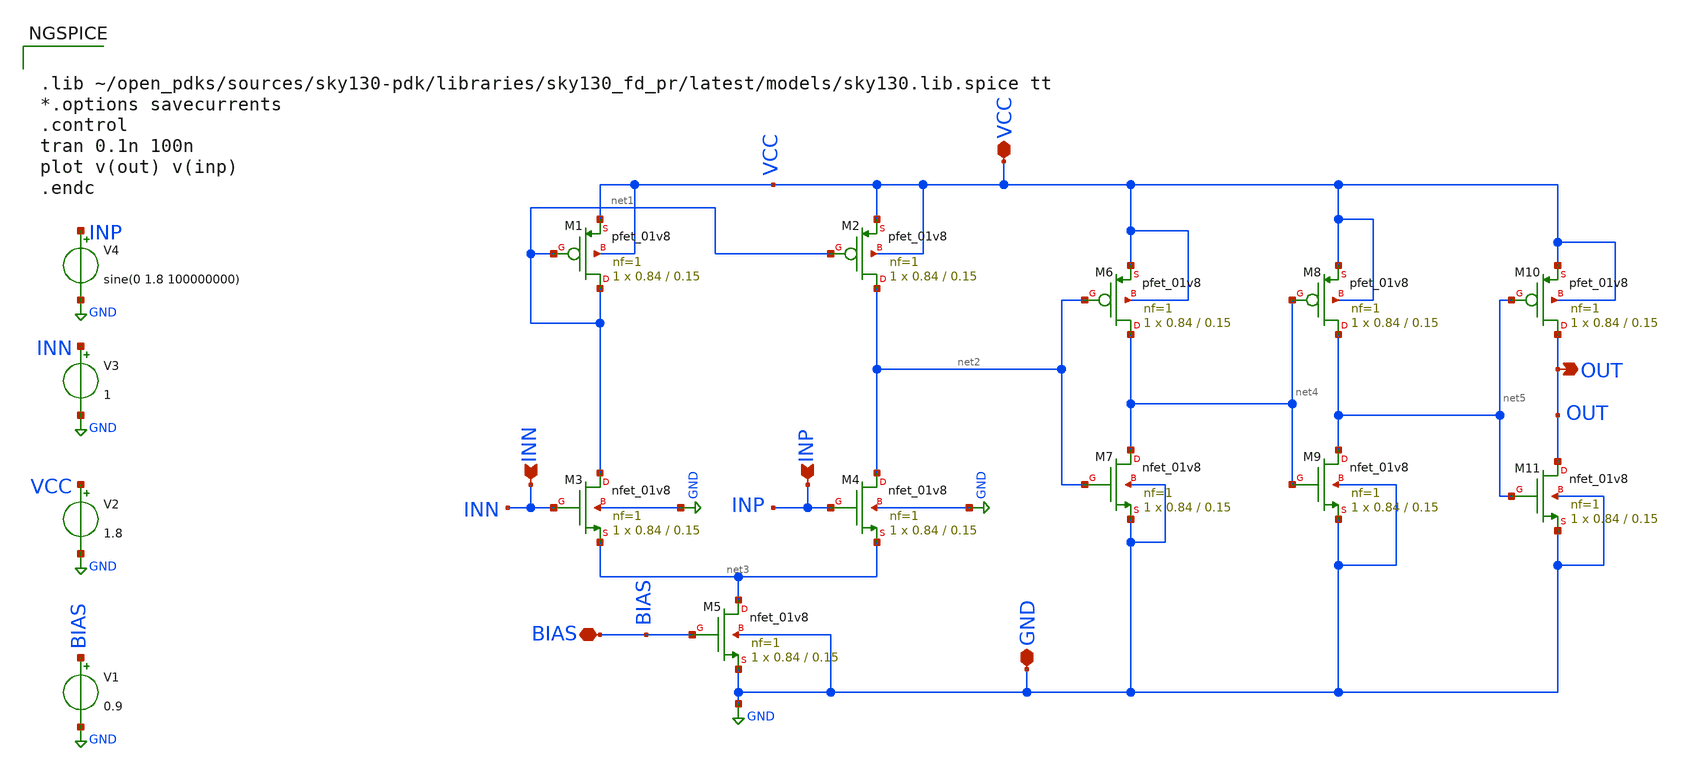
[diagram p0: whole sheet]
** sch_path: Week 4/xschem_180/comp_150.sch
**.subckt comp_150 OUT VCC GND INP INN BIAS
*.opin OUT
*.iopin VCC
*.iopin GND
*.ipin INP
*.ipin INN
*.iopin BIAS
V2 VCC GND 1.8
V3 INN GND 1
V4 INP GND sine(0 1.8 100000000)
XM1 net1 net1 VCC VCC sky130_fd_pr__pfet_01v8 L=0.15 W=0.84 nf=1 ad='int((nf+1)/2) * W/nf * 0.29' as='int((nf+2)/2) * W/nf * 0.29'
+ pd='2*int((nf+1)/2) * (W/nf + 0.29)' ps='2*int((nf+2)/2) * (W/nf + 0.29)' nrd='0.29 / W' nrs='0.29 / W'
+ sa=0 sb=0 sd=0 mult=1 m=1
XM2 net2 net1 VCC VCC sky130_fd_pr__pfet_01v8 L=0.15 W=0.84 nf=1 ad='int((nf+1)/2) * W/nf * 0.29' as='int((nf+2)/2) * W/nf * 0.29'
+ pd='2*int((nf+1)/2) * (W/nf + 0.29)' ps='2*int((nf+2)/2) * (W/nf + 0.29)' nrd='0.29 / W' nrs='0.29 / W'
+ sa=0 sb=0 sd=0 mult=1 m=1
XM3 net1 INN net3 GND sky130_fd_pr__nfet_01v8 L=0.15 W=0.84 nf=1 ad='int((nf+1)/2) * W/nf * 0.29' as='int((nf+2)/2) * W/nf * 0.29'
+ pd='2*int((nf+1)/2) * (W/nf + 0.29)' ps='2*int((nf+2)/2) * (W/nf + 0.29)' nrd='0.29 / W' nrs='0.29 / W'
+ sa=0 sb=0 sd=0 mult=1 m=1
XM4 net2 INP net3 GND sky130_fd_pr__nfet_01v8 L=0.15 W=0.84 nf=1 ad='int((nf+1)/2) * W/nf * 0.29' as='int((nf+2)/2) * W/nf * 0.29'
+ pd='2*int((nf+1)/2) * (W/nf + 0.29)' ps='2*int((nf+2)/2) * (W/nf + 0.29)' nrd='0.29 / W' nrs='0.29 / W'
+ sa=0 sb=0 sd=0 mult=1 m=1
XM5 net3 BIAS GND GND sky130_fd_pr__nfet_01v8 L=0.15 W=0.84 nf=1 ad='int((nf+1)/2) * W/nf * 0.29' as='int((nf+2)/2) * W/nf * 0.29'
+ pd='2*int((nf+1)/2) * (W/nf + 0.29)' ps='2*int((nf+2)/2) * (W/nf + 0.29)' nrd='0.29 / W' nrs='0.29 / W'
+ sa=0 sb=0 sd=0 mult=1 m=1
V1 BIAS GND 0.9
XM6 net4 net2 VCC VCC sky130_fd_pr__pfet_01v8 L=0.15 W=0.84 nf=1 ad='int((nf+1)/2) * W/nf * 0.29' as='int((nf+2)/2) * W/nf * 0.29'
+ pd='2*int((nf+1)/2) * (W/nf + 0.29)' ps='2*int((nf+2)/2) * (W/nf + 0.29)' nrd='0.29 / W' nrs='0.29 / W'
+ sa=0 sb=0 sd=0 mult=1 m=1
XM7 net4 net2 GND GND sky130_fd_pr__nfet_01v8 L=0.15 W=0.84 nf=1 ad='int((nf+1)/2) * W/nf * 0.29' as='int((nf+2)/2) * W/nf * 0.29'
+ pd='2*int((nf+1)/2) * (W/nf + 0.29)' ps='2*int((nf+2)/2) * (W/nf + 0.29)' nrd='0.29 / W' nrs='0.29 / W'
+ sa=0 sb=0 sd=0 mult=1 m=1
XM8 net5 net4 VCC VCC sky130_fd_pr__pfet_01v8 L=0.15 W=0.84 nf=1 ad='int((nf+1)/2) * W/nf * 0.29' as='int((nf+2)/2) * W/nf * 0.29'
+ pd='2*int((nf+1)/2) * (W/nf + 0.29)' ps='2*int((nf+2)/2) * (W/nf + 0.29)' nrd='0.29 / W' nrs='0.29 / W'
+ sa=0 sb=0 sd=0 mult=1 m=1
XM9 net5 net4 GND GND sky130_fd_pr__nfet_01v8 L=0.15 W=0.84 nf=1 ad='int((nf+1)/2) * W/nf * 0.29' as='int((nf+2)/2) * W/nf * 0.29'
+ pd='2*int((nf+1)/2) * (W/nf + 0.29)' ps='2*int((nf+2)/2) * (W/nf + 0.29)' nrd='0.29 / W' nrs='0.29 / W'
+ sa=0 sb=0 sd=0 mult=1 m=1
XM10 OUT net5 VCC VCC sky130_fd_pr__pfet_01v8 L=0.15 W=0.84 nf=1 ad='int((nf+1)/2) * W/nf * 0.29' as='int((nf+2)/2) * W/nf * 0.29'
+ pd='2*int((nf+1)/2) * (W/nf + 0.29)' ps='2*int((nf+2)/2) * (W/nf + 0.29)' nrd='0.29 / W' nrs='0.29 / W'
+ sa=0 sb=0 sd=0 mult=1 m=1
XM11 OUT net5 GND GND sky130_fd_pr__nfet_01v8 L=0.15 W=0.84 nf=1 ad='int((nf+1)/2) * W/nf * 0.29' as='int((nf+2)/2) * W/nf * 0.29'
+ pd='2*int((nf+1)/2) * (W/nf + 0.29)' ps='2*int((nf+2)/2) * (W/nf + 0.29)' nrd='0.29 / W' nrs='0.29 / W'
+ sa=0 sb=0 sd=0 mult=1 m=1
**** begin user architecture code


.lib ~/open_pdks/sources/sky130-pdk/libraries/sky130_fd_pr/latest/models/sky130.lib.spice tt
*.options savecurrents
.control
tran 0.1n 100n
plot v(out) v(inp)
.endc


**** end user architecture code
**.ends
.GLOBAL GND
.end
